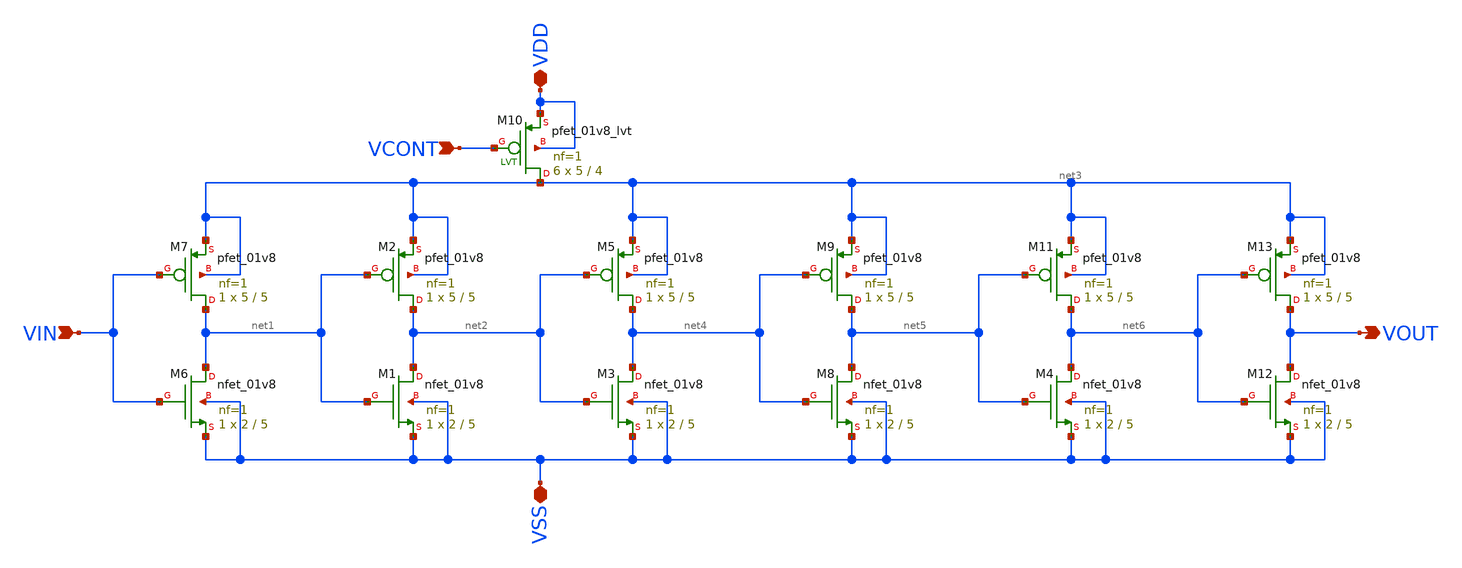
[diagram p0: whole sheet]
** sch_path: xschem/VCDL_HD_v1p1.sch
**.subckt VCDL_HD_v1p1 VIN VOUT VDD VSS VCONT
*.ipin VIN
*.opin VOUT
*.iopin VDD
*.iopin VSS
*.ipin VCONT
XM1 net2 net1 VSS VSS sky130_fd_pr__nfet_01v8 L=5 W=2 nf=1 ad='int((nf+1)/2) * W/nf * 0.29' as='int((nf+2)/2) * W/nf * 0.29'
+ pd='2*int((nf+1)/2) * (W/nf + 0.29)' ps='2*int((nf+2)/2) * (W/nf + 0.29)' nrd='0.29 / W' nrs='0.29 / W'
+ sa=0 sb=0 sd=0 mult=1 m=1
XM2 net2 net1 net3 net3 sky130_fd_pr__pfet_01v8 L=5 W=5 nf=1 ad='int((nf+1)/2) * W/nf * 0.29' as='int((nf+2)/2) * W/nf * 0.29'
+ pd='2*int((nf+1)/2) * (W/nf + 0.29)' ps='2*int((nf+2)/2) * (W/nf + 0.29)' nrd='0.29 / W' nrs='0.29 / W'
+ sa=0 sb=0 sd=0 mult=1 m=1
XM3 net4 net2 VSS VSS sky130_fd_pr__nfet_01v8 L=5 W=2 nf=1 ad='int((nf+1)/2) * W/nf * 0.29' as='int((nf+2)/2) * W/nf * 0.29'
+ pd='2*int((nf+1)/2) * (W/nf + 0.29)' ps='2*int((nf+2)/2) * (W/nf + 0.29)' nrd='0.29 / W' nrs='0.29 / W'
+ sa=0 sb=0 sd=0 mult=1 m=1
XM5 net4 net2 net3 net3 sky130_fd_pr__pfet_01v8 L=5 W=5 nf=1 ad='int((nf+1)/2) * W/nf * 0.29' as='int((nf+2)/2) * W/nf * 0.29'
+ pd='2*int((nf+1)/2) * (W/nf + 0.29)' ps='2*int((nf+2)/2) * (W/nf + 0.29)' nrd='0.29 / W' nrs='0.29 / W'
+ sa=0 sb=0 sd=0 mult=1 m=1
XM6 net1 VIN VSS VSS sky130_fd_pr__nfet_01v8 L=5 W=2 nf=1 ad='int((nf+1)/2) * W/nf * 0.29' as='int((nf+2)/2) * W/nf * 0.29'
+ pd='2*int((nf+1)/2) * (W/nf + 0.29)' ps='2*int((nf+2)/2) * (W/nf + 0.29)' nrd='0.29 / W' nrs='0.29 / W'
+ sa=0 sb=0 sd=0 mult=1 m=1
XM7 net1 VIN net3 net3 sky130_fd_pr__pfet_01v8 L=5 W=5 nf=1 ad='int((nf+1)/2) * W/nf * 0.29' as='int((nf+2)/2) * W/nf * 0.29'
+ pd='2*int((nf+1)/2) * (W/nf + 0.29)' ps='2*int((nf+2)/2) * (W/nf + 0.29)' nrd='0.29 / W' nrs='0.29 / W'
+ sa=0 sb=0 sd=0 mult=1 m=1
XM8 net5 net4 VSS VSS sky130_fd_pr__nfet_01v8 L=5 W=2 nf=1 ad='int((nf+1)/2) * W/nf * 0.29' as='int((nf+2)/2) * W/nf * 0.29'
+ pd='2*int((nf+1)/2) * (W/nf + 0.29)' ps='2*int((nf+2)/2) * (W/nf + 0.29)' nrd='0.29 / W' nrs='0.29 / W'
+ sa=0 sb=0 sd=0 mult=1 m=1
XM9 net5 net4 net3 net3 sky130_fd_pr__pfet_01v8 L=5 W=5 nf=1 ad='int((nf+1)/2) * W/nf * 0.29' as='int((nf+2)/2) * W/nf * 0.29'
+ pd='2*int((nf+1)/2) * (W/nf + 0.29)' ps='2*int((nf+2)/2) * (W/nf + 0.29)' nrd='0.29 / W' nrs='0.29 / W'
+ sa=0 sb=0 sd=0 mult=1 m=1
XM10 net3 VCONT VDD VDD sky130_fd_pr__pfet_01v8_lvt L=4 W=5 nf=1 ad='int((nf+1)/2) * W/nf * 0.29' as='int((nf+2)/2) * W/nf * 0.29'
+ pd='2*int((nf+1)/2) * (W/nf + 0.29)' ps='2*int((nf+2)/2) * (W/nf + 0.29)' nrd='0.29 / W' nrs='0.29 / W'
+ sa=0 sb=0 sd=0 mult=6 m=6
XM4 net6 net5 VSS VSS sky130_fd_pr__nfet_01v8 L=5 W=2 nf=1 ad='int((nf+1)/2) * W/nf * 0.29' as='int((nf+2)/2) * W/nf * 0.29'
+ pd='2*int((nf+1)/2) * (W/nf + 0.29)' ps='2*int((nf+2)/2) * (W/nf + 0.29)' nrd='0.29 / W' nrs='0.29 / W'
+ sa=0 sb=0 sd=0 mult=1 m=1
XM11 net6 net5 net3 net3 sky130_fd_pr__pfet_01v8 L=5 W=5 nf=1 ad='int((nf+1)/2) * W/nf * 0.29' as='int((nf+2)/2) * W/nf * 0.29'
+ pd='2*int((nf+1)/2) * (W/nf + 0.29)' ps='2*int((nf+2)/2) * (W/nf + 0.29)' nrd='0.29 / W' nrs='0.29 / W'
+ sa=0 sb=0 sd=0 mult=1 m=1
XM12 VOUT net6 VSS VSS sky130_fd_pr__nfet_01v8 L=5 W=2 nf=1 ad='int((nf+1)/2) * W/nf * 0.29' as='int((nf+2)/2) * W/nf * 0.29'
+ pd='2*int((nf+1)/2) * (W/nf + 0.29)' ps='2*int((nf+2)/2) * (W/nf + 0.29)' nrd='0.29 / W' nrs='0.29 / W'
+ sa=0 sb=0 sd=0 mult=1 m=1
XM13 VOUT net6 net3 net3 sky130_fd_pr__pfet_01v8 L=5 W=5 nf=1 ad='int((nf+1)/2) * W/nf * 0.29' as='int((nf+2)/2) * W/nf * 0.29'
+ pd='2*int((nf+1)/2) * (W/nf + 0.29)' ps='2*int((nf+2)/2) * (W/nf + 0.29)' nrd='0.29 / W' nrs='0.29 / W'
+ sa=0 sb=0 sd=0 mult=1 m=1
**.ends
.end
